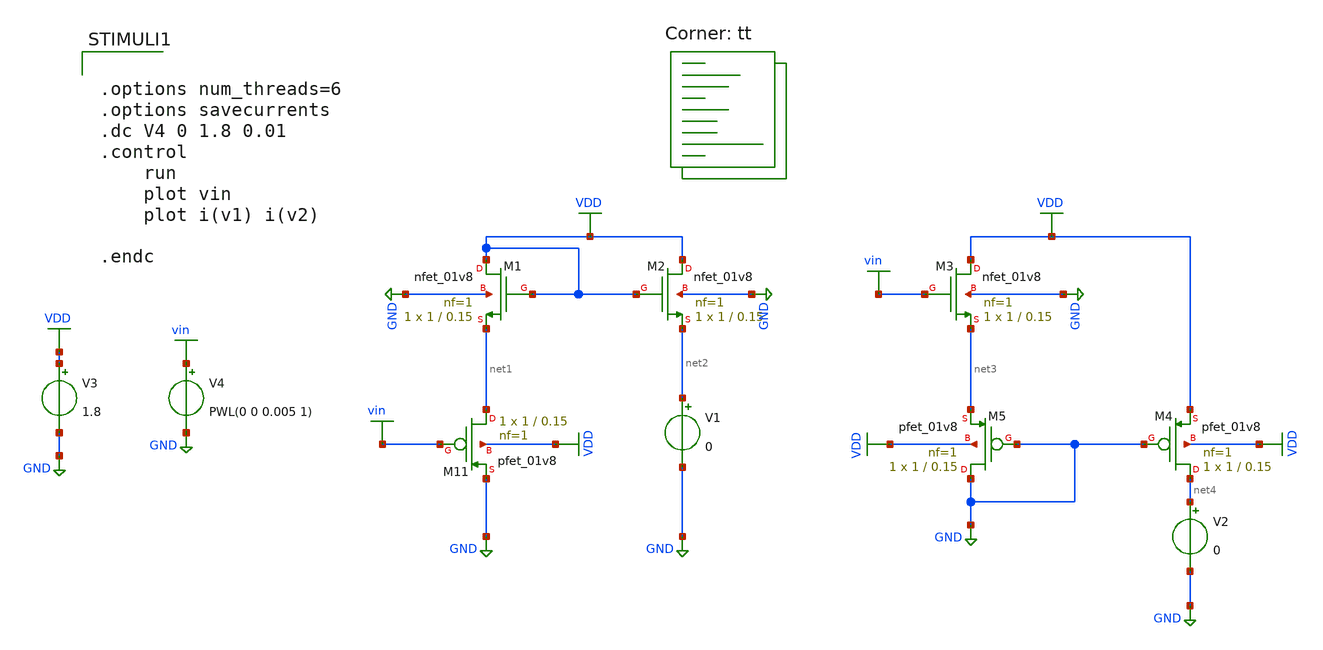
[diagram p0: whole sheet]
** sch_path: tb_curr_scs.sch
**.subckt tb_curr_scs
XM2 VDD VDD net2 GND sky130_fd_pr__nfet_01v8 L=0.15 W=1 nf=1 ad='int((1 + 1)/2) * 1 / 1 * 0.29' as='int((1 + 2)/2) * 1 / 1 * 0.29'
+ pd='2*int((1 + 1)/2) * (1 / 1 + 0.29)' ps='2*int((1 + 2)/2) * (1 / 1 + 0.29)' nrd='0.29 / 1 ' nrs='0.29 / 1 '
+ sa=0 sb=0 sd=0 mult=1 m=1
XM1 VDD VDD net1 GND sky130_fd_pr__nfet_01v8 L=0.15 W=1 nf=1 ad='int((1 + 1)/2) * 1 / 1 * 0.29' as='int((1 + 2)/2) * 1 / 1 * 0.29'
+ pd='2*int((1 + 1)/2) * (1 / 1 + 0.29)' ps='2*int((1 + 2)/2) * (1 / 1 + 0.29)' nrd='0.29 / 1 ' nrs='0.29 / 1 '
+ sa=0 sb=0 sd=0 mult=1 m=1
XM11 net1 vin GND VDD sky130_fd_pr__pfet_01v8 L=0.15 W=1 nf=1 ad='int((nf+1)/2) * W/nf * 0.29' as='int((nf+2)/2) * W/nf * 0.29'
+ pd='2*int((nf+1)/2) * (W/nf + 0.29)' ps='2*int((nf+2)/2) * (W/nf + 0.29)' nrd='0.29 / W' nrs='0.29 / W'
+ sa=0 sb=0 sd=0 mult=1 m=1
XM3 VDD vin net3 GND sky130_fd_pr__nfet_01v8 L=0.15 W=1 nf=1 ad='int((1 + 1)/2) * 1 / 1 * 0.29' as='int((1 + 2)/2) * 1 / 1 * 0.29'
+ pd='2*int((1 + 1)/2) * (1 / 1 + 0.29)' ps='2*int((1 + 2)/2) * (1 / 1 + 0.29)' nrd='0.29 / 1 ' nrs='0.29 / 1 '
+ sa=0 sb=0 sd=0 mult=1 m=1
XM4 net4 GND VDD VDD sky130_fd_pr__pfet_01v8 L=0.15 W=1 nf=1 ad='int((nf+1)/2) * W/nf * 0.29' as='int((nf+2)/2) * W/nf * 0.29'
+ pd='2*int((nf+1)/2) * (W/nf + 0.29)' ps='2*int((nf+2)/2) * (W/nf + 0.29)' nrd='0.29 / W' nrs='0.29 / W'
+ sa=0 sb=0 sd=0 mult=1 m=1
XM5 GND GND net3 VDD sky130_fd_pr__pfet_01v8 L=0.15 W=1 nf=1 ad='int((nf+1)/2) * W/nf * 0.29' as='int((nf+2)/2) * W/nf * 0.29'
+ pd='2*int((nf+1)/2) * (W/nf + 0.29)' ps='2*int((nf+2)/2) * (W/nf + 0.29)' nrd='0.29 / W' nrs='0.29 / W'
+ sa=0 sb=0 sd=0 mult=1 m=1
V3 VDD GND 1.8
V4 vin GND PWL(0 0 0.005 1)
V1 net2 GND 0
V2 net4 GND 0
**** begin user architecture code
.lib $::SKYWATER_MODELS/sky130.lib.spice tt
**** end user architecture code
**.ends
.GLOBAL VDD
.GLOBAL GND
.GLOBAL vin
**** begin user architecture code


.options num_threads=6
.options savecurrents
.dc V4 0 1.8 0.01
.control
	run
	plot vin
	plot i(v1) i(v2)

.endc


**** end user architecture code
.end
